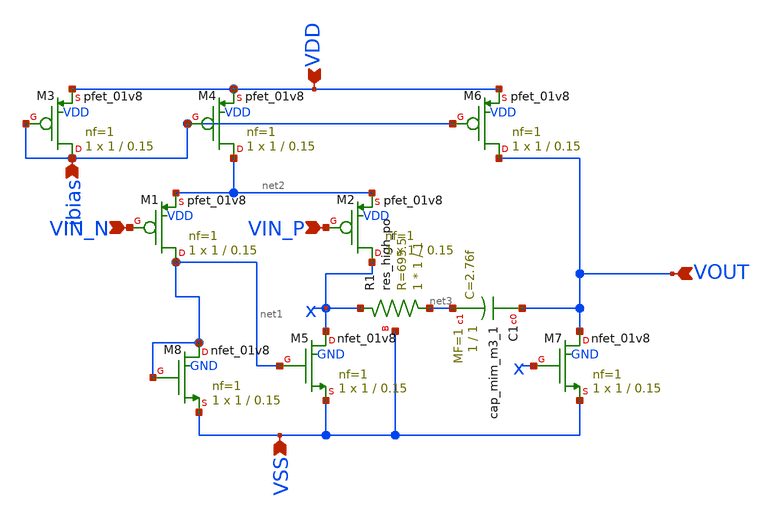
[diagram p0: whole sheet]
** sch_path: analog/bootcamp_opamp/schematics/opamp_two_stage.sch
**.subckt opamp_two_stage VDD VSS VOUT VIN_P VIN_N ibias
*.ipin VDD
*.ipin VSS
*.ipin VOUT
*.ipin VIN_P
*.ipin VIN_N
*.ipin ibias
XM3 ibias ibias VDD VDD sky130_fd_pr__pfet_01v8 L=0.15 W=1 nf=1 ad='int((nf+1)/2) * W/nf * 0.29' as='int((nf+2)/2) * W/nf * 0.29'
+ pd='2*int((nf+1)/2) * (W/nf + 0.29)' ps='2*int((nf+2)/2) * (W/nf + 0.29)' nrd='0.29 / W' nrs='0.29 / W'
+ sa=0 sb=0 sd=0 mult=1 m=1
XM4 net2 ibias VDD VDD sky130_fd_pr__pfet_01v8 L=0.15 W=1 nf=1 ad='int((nf+1)/2) * W/nf * 0.29' as='int((nf+2)/2) * W/nf * 0.29'
+ pd='2*int((nf+1)/2) * (W/nf + 0.29)' ps='2*int((nf+2)/2) * (W/nf + 0.29)' nrd='0.29 / W' nrs='0.29 / W'
+ sa=0 sb=0 sd=0 mult=1 m=1
XM5 x net1 VSS GND sky130_fd_pr__nfet_01v8 L=0.15 W=1 nf=1 ad='int((nf+1)/2) * W/nf * 0.29' as='int((nf+2)/2) * W/nf * 0.29'
+ pd='2*int((nf+1)/2) * (W/nf + 0.29)' ps='2*int((nf+2)/2) * (W/nf + 0.29)' nrd='0.29 / W' nrs='0.29 / W'
+ sa=0 sb=0 sd=0 mult=1 m=1
XM6 VOUT ibias VDD VDD sky130_fd_pr__pfet_01v8 L=0.15 W=1 nf=1 ad='int((nf+1)/2) * W/nf * 0.29' as='int((nf+2)/2) * W/nf * 0.29'
+ pd='2*int((nf+1)/2) * (W/nf + 0.29)' ps='2*int((nf+2)/2) * (W/nf + 0.29)' nrd='0.29 / W' nrs='0.29 / W'
+ sa=0 sb=0 sd=0 mult=1 m=1
XM7 VOUT x VSS GND sky130_fd_pr__nfet_01v8 L=0.15 W=1 nf=1 ad='int((nf+1)/2) * W/nf * 0.29' as='int((nf+2)/2) * W/nf * 0.29'
+ pd='2*int((nf+1)/2) * (W/nf + 0.29)' ps='2*int((nf+2)/2) * (W/nf + 0.29)' nrd='0.29 / W' nrs='0.29 / W'
+ sa=0 sb=0 sd=0 mult=1 m=1
XM8 net1 net1 VSS GND sky130_fd_pr__nfet_01v8 L=0.15 W=1 nf=1 ad='int((nf+1)/2) * W/nf * 0.29' as='int((nf+2)/2) * W/nf * 0.29'
+ pd='2*int((nf+1)/2) * (W/nf + 0.29)' ps='2*int((nf+2)/2) * (W/nf + 0.29)' nrd='0.29 / W' nrs='0.29 / W'
+ sa=0 sb=0 sd=0 mult=1 m=1
XR1 net3 x VSS sky130_fd_pr__res_high_po W=1 L=1 mult=1 m=1
XC1 VOUT net3 sky130_fd_pr__cap_mim_m3_1 W=1 L=1 MF=1 m=1
XM1 net1 VIN_N net2 VDD sky130_fd_pr__pfet_01v8 L=0.15 W=1 nf=1 ad='int((nf+1)/2) * W/nf * 0.29' as='int((nf+2)/2) * W/nf * 0.29'
+ pd='2*int((nf+1)/2) * (W/nf + 0.29)' ps='2*int((nf+2)/2) * (W/nf + 0.29)' nrd='0.29 / W' nrs='0.29 / W'
+ sa=0 sb=0 sd=0 mult=1 m=1
XM2 x VIN_P net2 VDD sky130_fd_pr__pfet_01v8 L=0.15 W=1 nf=1 ad='int((nf+1)/2) * W/nf * 0.29' as='int((nf+2)/2) * W/nf * 0.29'
+ pd='2*int((nf+1)/2) * (W/nf + 0.29)' ps='2*int((nf+2)/2) * (W/nf + 0.29)' nrd='0.29 / W' nrs='0.29 / W'
+ sa=0 sb=0 sd=0 mult=1 m=1
**.ends
.end
